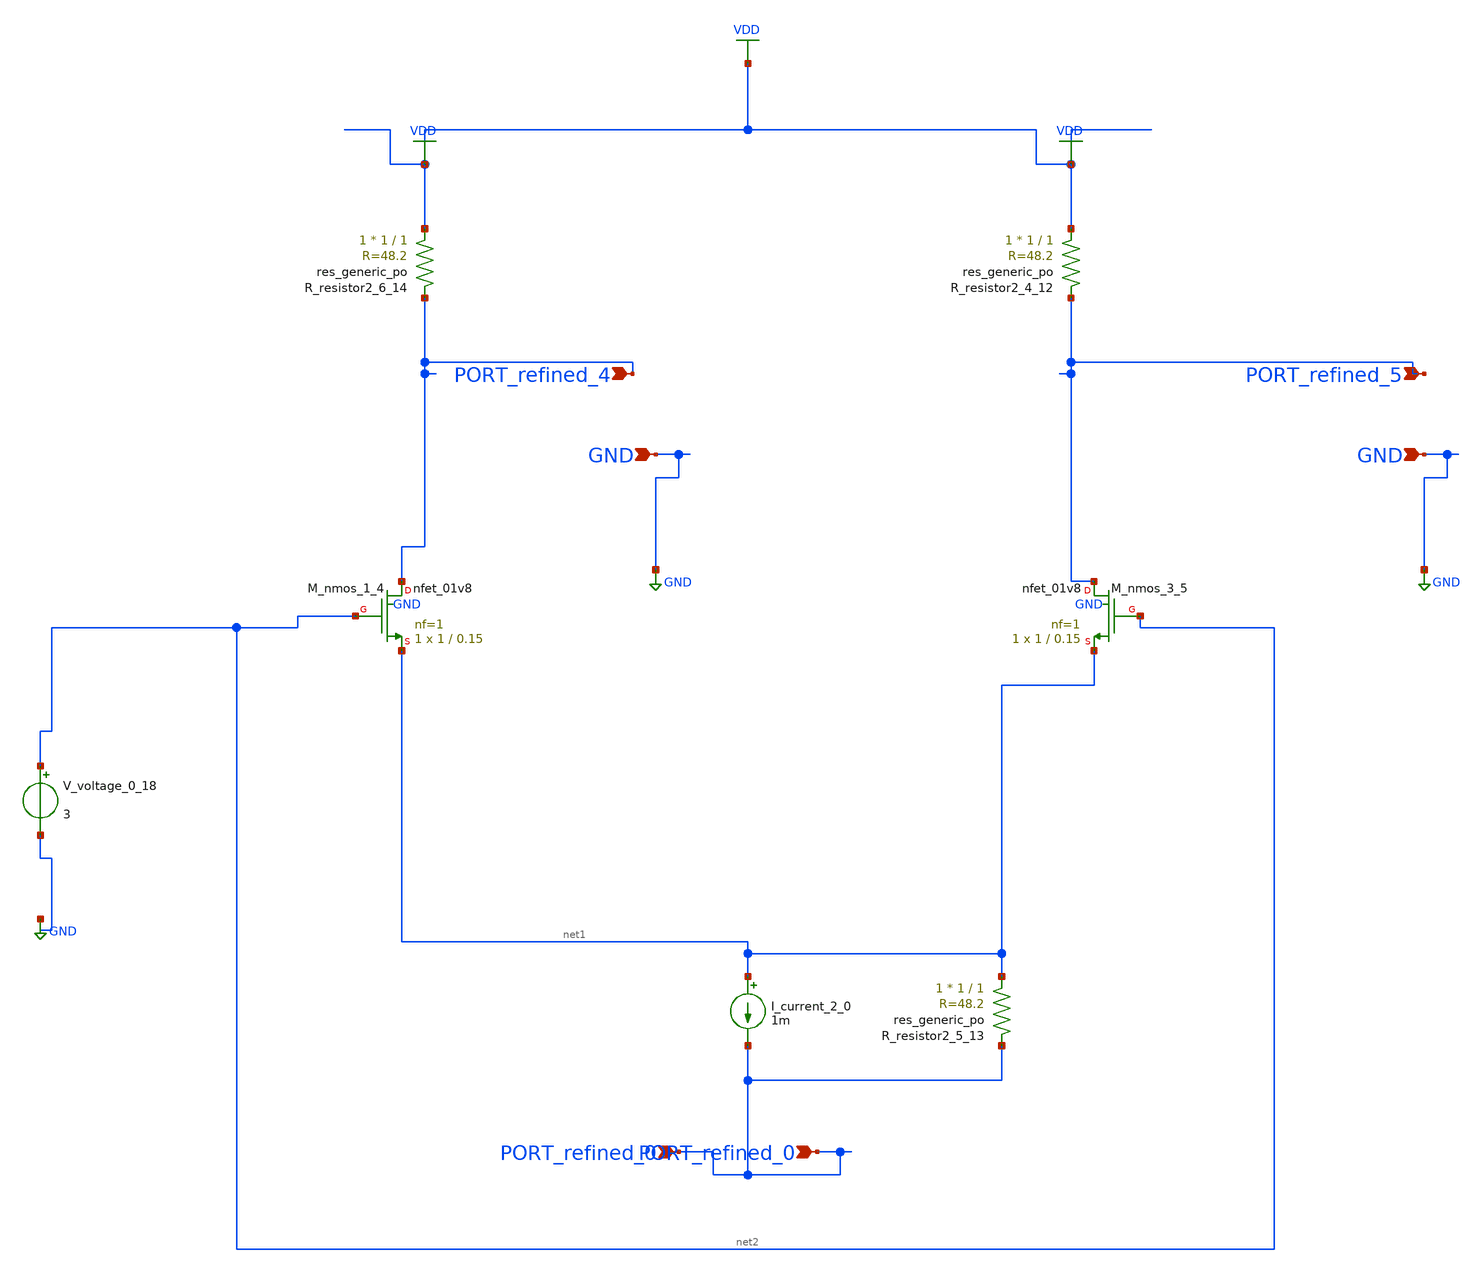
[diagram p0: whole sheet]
** sch_path: schematics/Image2Net/003.sch
**.subckt 003 GND GND PORT_refined_4 PORT_refined_5 PORT_refined_0 PORT_refined_0
*.ipin GND
*.ipin GND
*.ipin PORT_refined_4
*.ipin PORT_refined_5
*.ipin PORT_refined_0
*.ipin PORT_refined_0
I_current_2_0 net1 PORT_refined_0 1m
XM_nmos_1_4 PORT_refined_4 net2 net1 GND sky130_fd_pr__nfet_01v8 L=0.15 W=1 nf=1 ad='int((1 + 1)/2) * 1 / 1 * 0.29'
+ as='int((1 + 2)/2) * 1 / 1 * 0.29' pd='2*int((1 + 1)/2) * (1 / 1 + 0.29)' ps='2*int((1 + 2)/2) * (1 / 1 + 0.29)'
+ nrd='0.29 / 1 ' nrs='0.29 / 1 ' sa=0 sb=0 sd=0 mult=1 m=1
XM_nmos_3_5 PORT_refined_5 net2 net1 GND sky130_fd_pr__nfet_01v8 L=0.15 W=1 nf=1 ad='int((1 + 1)/2) * 1 / 1 * 0.29'
+ as='int((1 + 2)/2) * 1 / 1 * 0.29' pd='2*int((1 + 1)/2) * (1 / 1 + 0.29)' ps='2*int((1 + 2)/2) * (1 / 1 + 0.29)'
+ nrd='0.29 / 1 ' nrs='0.29 / 1 ' sa=0 sb=0 sd=0 mult=1 m=1
XR_resistor2_4_12 VDD PORT_refined_5 sky130_fd_pr__res_generic_po W=1 L=1 m=1
XR_resistor2_5_13 net1 PORT_refined_0 sky130_fd_pr__res_generic_po W=1 L=1 m=1
XR_resistor2_6_14 VDD PORT_refined_4 sky130_fd_pr__res_generic_po W=1 L=1 m=1
V_voltage_0_18 net2 GND 3
**.ends
.GLOBAL GND
.GLOBAL VDD
.end
